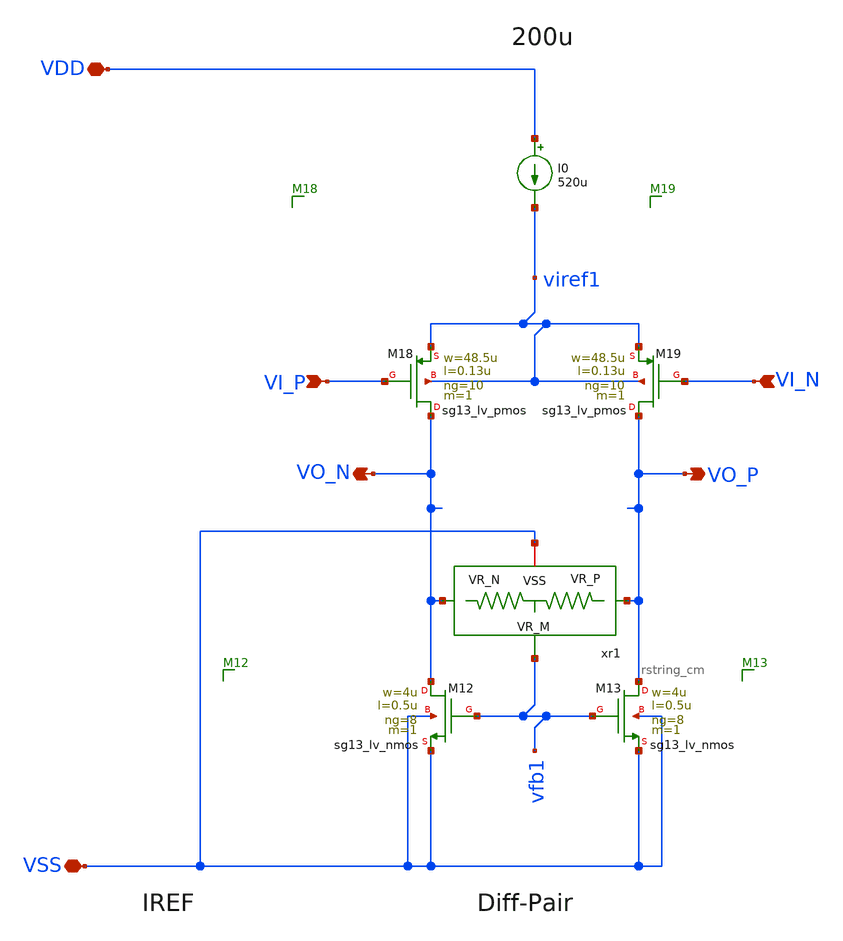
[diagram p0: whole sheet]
** sch_path: macros/filter_cmos5l/schematic/xschem/amp_input_stage.sch
**.subckt amp_input_stage VSS VDD VI_P VI_N VO_N VO_P
*.iopin VSS
*.iopin VDD
*.ipin VI_P
*.ipin VI_N
*.opin VO_N
*.opin VO_P
XM12 VO_N vfb1 VSS VSS sg13_lv_nmos w=4u l=0.5u ng=8 m=1 mm_ok=1
XM13 VO_P vfb1 VSS VSS sg13_lv_nmos w=4u l=0.5u ng=8 m=1 mm_ok=1
XM18 VO_N VI_P viref1 viref1 sg13_lv_pmos w=48.5u l=0.13u ng=10 m=1 mm_ok=1
XM19 VO_P VI_N viref1 viref1 sg13_lv_pmos w=48.5u l=0.13u ng=10 m=1 mm_ok=1
I0 VDD viref1 520u
xr1 vfb1 VO_N VO_P VSS rstring_cm
**.ends

* expanding   symbol:  rstring_cm.sym # of pins=4
** sym_path: rstring_cm.sym
** sch_path: rstring_cm.sch
.subckt rstring_cm VR_M VR_N VR_P VSS
*.iopin VSS
*.ipin VR_P
*.ipin VR_N
*.opin VR_M
R1 VR_P VR_M 1Meg m=1
R4 VR_M VR_N 1Meg m=1
.ends

.end
